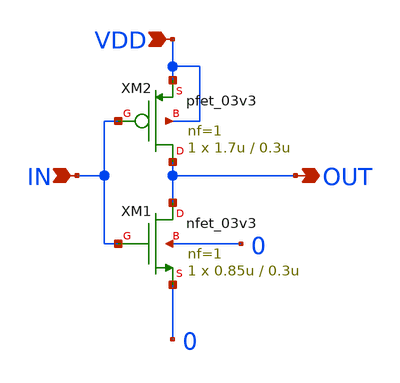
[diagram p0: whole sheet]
** sch_path: chipathon_2023/initial_notebooks_2023/accepted_notebooks/Current-Steering-DAC/DAC/inveter.sch
**.subckt inveter VDD OUT IN
*.ipin VDD
*.opin OUT
*.ipin IN
XM2 OUT IN VDD VDD pfet_03v3 L=0.3u W=1.7u nf=1 ad='int((nf+1)/2) * W/nf * 0.18u' as='int((nf+2)/2) * W/nf * 0.18u'
+ pd='2*int((nf+1)/2) * (W/nf + 0.18u)' ps='2*int((nf+2)/2) * (W/nf + 0.18u)' nrd='0.18u / W' nrs='0.18u / W'
+ sa=0 sb=0 sd=0 m=1
XM1 OUT IN 0 0 nfet_03v3 L=0.3u W=0.85u nf=1 ad='int((nf+1)/2) * W/nf * 0.18u' as='int((nf+2)/2) * W/nf * 0.18u'
+ pd='2*int((nf+1)/2) * (W/nf + 0.18u)' ps='2*int((nf+2)/2) * (W/nf + 0.18u)' nrd='0.18u / W' nrs='0.18u / W'
+ sa=0 sb=0 sd=0 m=1
**.ends
.end
